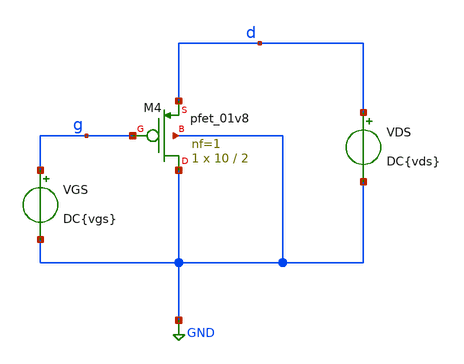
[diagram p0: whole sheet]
** sch_path: tp1_2.sch
**.subckt tp1_2
VGS g GND DC{vgs}
VDS d GND DC{vds}
XM4 GND g d GND sky130_fd_pr__pfet_01v8 L=2 W=10 nf=1 ad='int((nf+1)/2) * W/nf * 0.29' as='int((nf+2)/2) * W/nf * 0.29'
+ pd='2*int((nf+1)/2) * (W/nf + 0.29)' ps='2*int((nf+2)/2) * (W/nf + 0.29)' nrd='0.29 / W' nrs='0.29 / W'
+ sa=0 sb=0 sd=0 mult=1 m=1
**** begin user architecture code



* Parameters
.param vds = -1.8
.param vgs = -0.9
.options TEMPS = 27.0

* Models
.lib ~/skywater/skywater-pdk/libraries/sky130_fd_pr_ngspice/latest/models/corners/sky130.lib TT

* Data to save
.save all  @M.XM4.msky130_fd_pr__pfet_01v8[id]  @M.XM4.msky130_fd_pr__pfet_01v8[gm]  @M.XM4.msky130_fd_pr__pfet_01v8[vth]  @M.XM4.msky130_fd_pr__pfet_01v8[vds]  @M.XM4.msky130_fd_pr__pfet_01v8[vdsat]  @M.XM4.msky130_fd_pr__pfet_01v8[vgs]


* Simulation
 .control
  dc VGS -1.8 0 0.01
  setplot dc7
  plot -@M.XM4.msky130_fd_pr__pfet_01v8[id] ylabel Id xlabel Vgs title 'Id vs Vgs'
  set filetype = ascii
  write tp1_1_dc7.raw

  reset
  dc VDS  -1.8 0 0.01 VGS -1.8 0 0.3
  setplot dc6
  plot -@M.XM4.msky130_fd_pr__pfet_01v8[id] ylabel Id xlabel Vds title 'Id vs Vds vs Vgs'
  set filetype = ascii
  write tp1_2_dc6.raw

.endc

.end


**** end user architecture code
**.ends
.GLOBAL GND
.end
